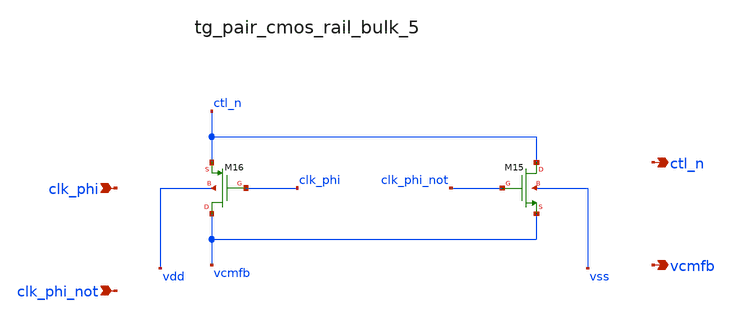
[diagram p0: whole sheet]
** sch_path: analog-db/raw/cmfb_004_output_switched_cap/hier/blocks/tg_pair_cmos_rail_bulk_5.sch
**.subckt tg_pair_cmos_rail_bulk_5 clk_phi clk_phi_not ctl_n vcmfb
*.ipin clk_phi
*.ipin clk_phi_not
*.opin ctl_n
*.opin vcmfb
XM15 ctl_n clk_phi_not vcmfb vss sg13_lv_nmos w=x_dut_xm15_w l=x_dut_xm15_l ng=1 m=x_dut_xm15_m
XM16 vcmfb clk_phi ctl_n vdd sg13_lv_pmos w=x_dut_xm16_w l=x_dut_xm16_l ng=1 m=x_dut_xm16_m
**.ends
.end
